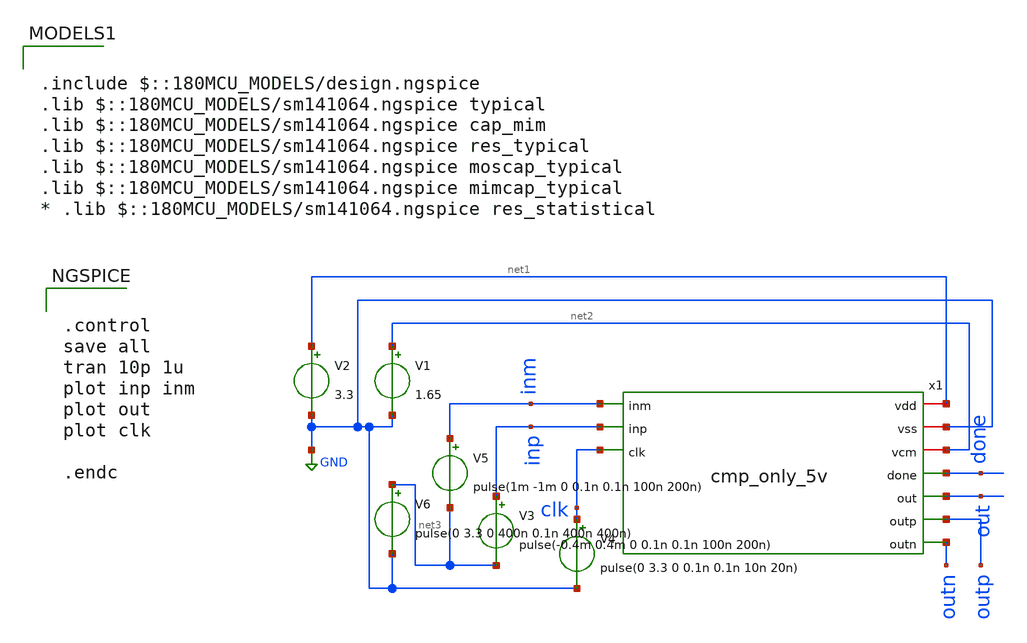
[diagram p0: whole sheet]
** sch_path: member_project/ice458/dynamic_comparator/xschem/cmp_only_tb_5v.sch
**.subckt cmp_only_tb_5v
x1 net1 GND net2 inm inp clk done out outp outn cmp_only_5v
V2 net1 GND 3.3
V1 net2 GND 1.65
V4 clk GND pulse(0 3.3 0 0.1n 0.1n 10n 20n)
V5 inm net3 pulse(1m -1m 0 0.1n 0.1n 100n 200n)
V3 inp net3 pulse(-0.4m 0.4m 0 0.1n 0.1n 100n 200n)
V6 net3 GND pulse(0 3.3 0 400n 0.1n 400n 400n)
**** begin user architecture code


.control
save all
tran 10p 1u
plot inp inm
plot out
plot clk

.endc



.include $::180MCU_MODELS/design.ngspice
.lib $::180MCU_MODELS/sm141064.ngspice typical
.lib $::180MCU_MODELS/sm141064.ngspice cap_mim
.lib $::180MCU_MODELS/sm141064.ngspice res_typical
.lib $::180MCU_MODELS/sm141064.ngspice moscap_typical
.lib $::180MCU_MODELS/sm141064.ngspice mimcap_typical
* .lib $::180MCU_MODELS/sm141064.ngspice res_statistical

**** end user architecture code
**.ends
.GLOBAL GND
.end
